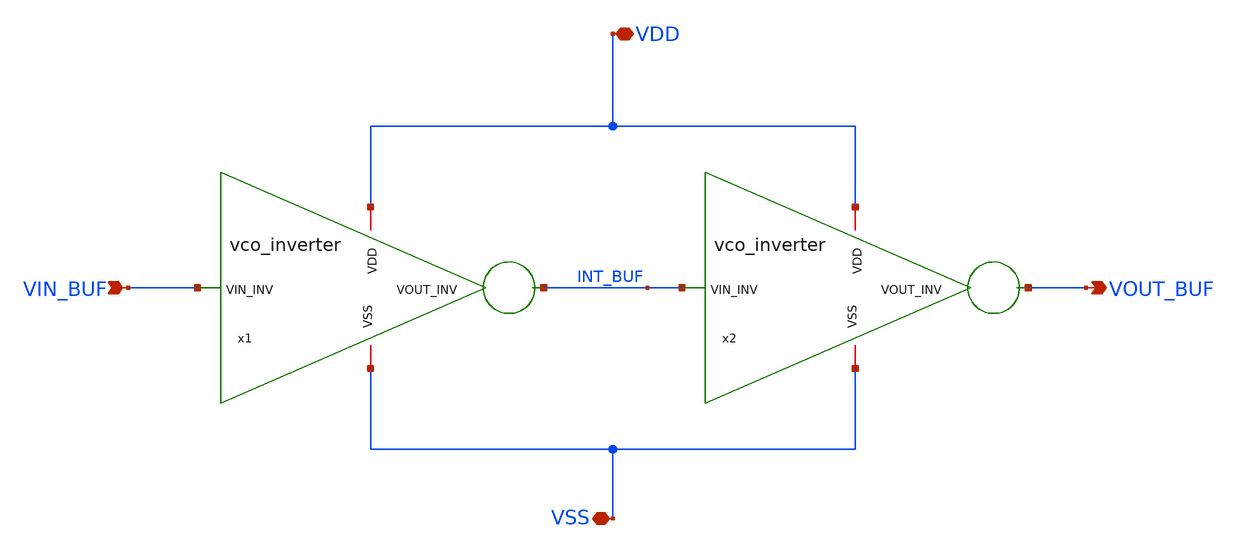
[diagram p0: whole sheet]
** sch_path: xschem/vco_buffer.sch
**.subckt vco_buffer VDD VSS VIN_BUF VOUT_BUF
*.iopin VDD
*.iopin VSS
*.ipin VIN_BUF
*.opin VOUT_BUF
x1 VDD VIN_BUF INT_BUF VSS vco_inverter
x2 VDD INT_BUF VOUT_BUF VSS vco_inverter
**.ends

* expanding   symbol:  vco_inverter.sym # of pins=4
** sym_path: xschem/vco_inverter.sym
** sch_path: xschem/vco_inverter.sch
.subckt vco_inverter VDD VIN_INV VOUT_INV VSS
*.iopin VDD
*.iopin VSS
*.ipin VIN_INV
*.opin VOUT_INV
XM1 VOUT_INV VIN_INV VSS VSS sky130_fd_pr__nfet_01v8 L=0.15 W=1 nf=1 ad='int((nf+1)/2) * W/nf * 0.29'
+ as='int((nf+2)/2) * W/nf * 0.29' pd='2*int((nf+1)/2) * (W/nf + 0.29)' ps='2*int((nf+2)/2) * (W/nf + 0.29)'
+ nrd='0.29 / W' nrs='0.29 / W' sa=0 sb=0 sd=0 mult=1 m=1
XM2 VOUT_INV VIN_INV VDD VDD sky130_fd_pr__pfet_01v8 L=0.15 W=1 nf=1 ad='int((nf+1)/2) * W/nf * 0.29'
+ as='int((nf+2)/2) * W/nf * 0.29' pd='2*int((nf+1)/2) * (W/nf + 0.29)' ps='2*int((nf+2)/2) * (W/nf + 0.29)'
+ nrd='0.29 / W' nrs='0.29 / W' sa=0 sb=0 sd=0 mult=1 m=1
.ends

.end
